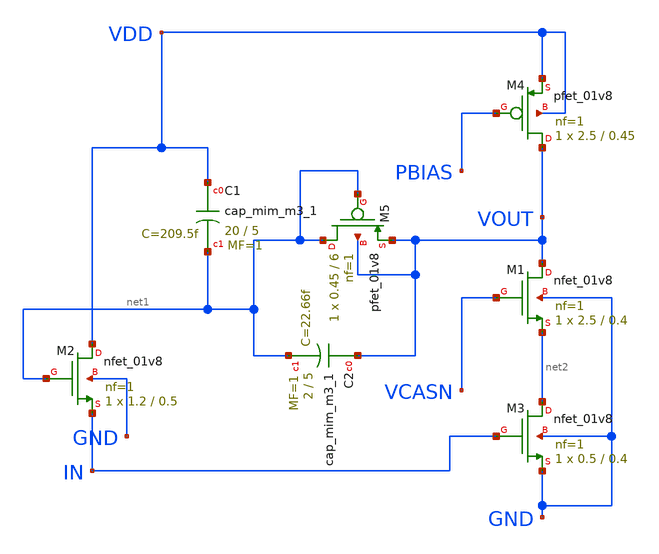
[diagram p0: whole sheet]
** sch_path: project3/tia/TIA.sch
**.subckt TIA
XC1 VDD net1 sky130_fd_pr__cap_mim_m3_1 W=20 L=5 MF=1 m=1
XC2 VOUT net1 sky130_fd_pr__cap_mim_m3_1 W=2 L=5 MF=1 m=1
XM1 VOUT VCASN net2 GND sky130_fd_pr__nfet_01v8 L=0.4 W=2.5 nf=1 ad='int((nf+1)/2) * W/nf * 0.29' as='int((nf+2)/2) * W/nf * 0.29'
+ pd='2*int((nf+1)/2) * (W/nf + 0.29)' ps='2*int((nf+2)/2) * (W/nf + 0.29)' nrd='0.29 / W' nrs='0.29 / W'
+ sa=0 sb=0 sd=0 mult=1 m=1
XM2 VDD net1 IN GND sky130_fd_pr__nfet_01v8 L=0.5 W=1.2 nf=1 ad='int((nf+1)/2) * W/nf * 0.29' as='int((nf+2)/2) * W/nf * 0.29'
+ pd='2*int((nf+1)/2) * (W/nf + 0.29)' ps='2*int((nf+2)/2) * (W/nf + 0.29)' nrd='0.29 / W' nrs='0.29 / W'
+ sa=0 sb=0 sd=0 mult=1 m=1
XM3 net2 IN GND GND sky130_fd_pr__nfet_01v8 L=0.4 W=0.5 nf=1 ad='int((nf+1)/2) * W/nf * 0.29' as='int((nf+2)/2) * W/nf * 0.29'
+ pd='2*int((nf+1)/2) * (W/nf + 0.29)' ps='2*int((nf+2)/2) * (W/nf + 0.29)' nrd='0.29 / W' nrs='0.29 / W'
+ sa=0 sb=0 sd=0 mult=1 m=1
XM4 VOUT PBIAS VDD VDD sky130_fd_pr__pfet_01v8 L=0.45 W=2.5 nf=1 ad='int((nf+1)/2) * W/nf * 0.29' as='int((nf+2)/2) * W/nf * 0.29'
+ pd='2*int((nf+1)/2) * (W/nf + 0.29)' ps='2*int((nf+2)/2) * (W/nf + 0.29)' nrd='0.29 / W' nrs='0.29 / W'
+ sa=0 sb=0 sd=0 mult=1 m=1
XM5 net1 net1 VOUT VOUT sky130_fd_pr__pfet_01v8 L=6 W=0.45 nf=1 ad='int((nf+1)/2) * W/nf * 0.29' as='int((nf+2)/2) * W/nf * 0.29'
+ pd='2*int((nf+1)/2) * (W/nf + 0.29)' ps='2*int((nf+2)/2) * (W/nf + 0.29)' nrd='0.29 / W' nrs='0.29 / W'
+ sa=0 sb=0 sd=0 mult=1 m=1
**.ends
.end
